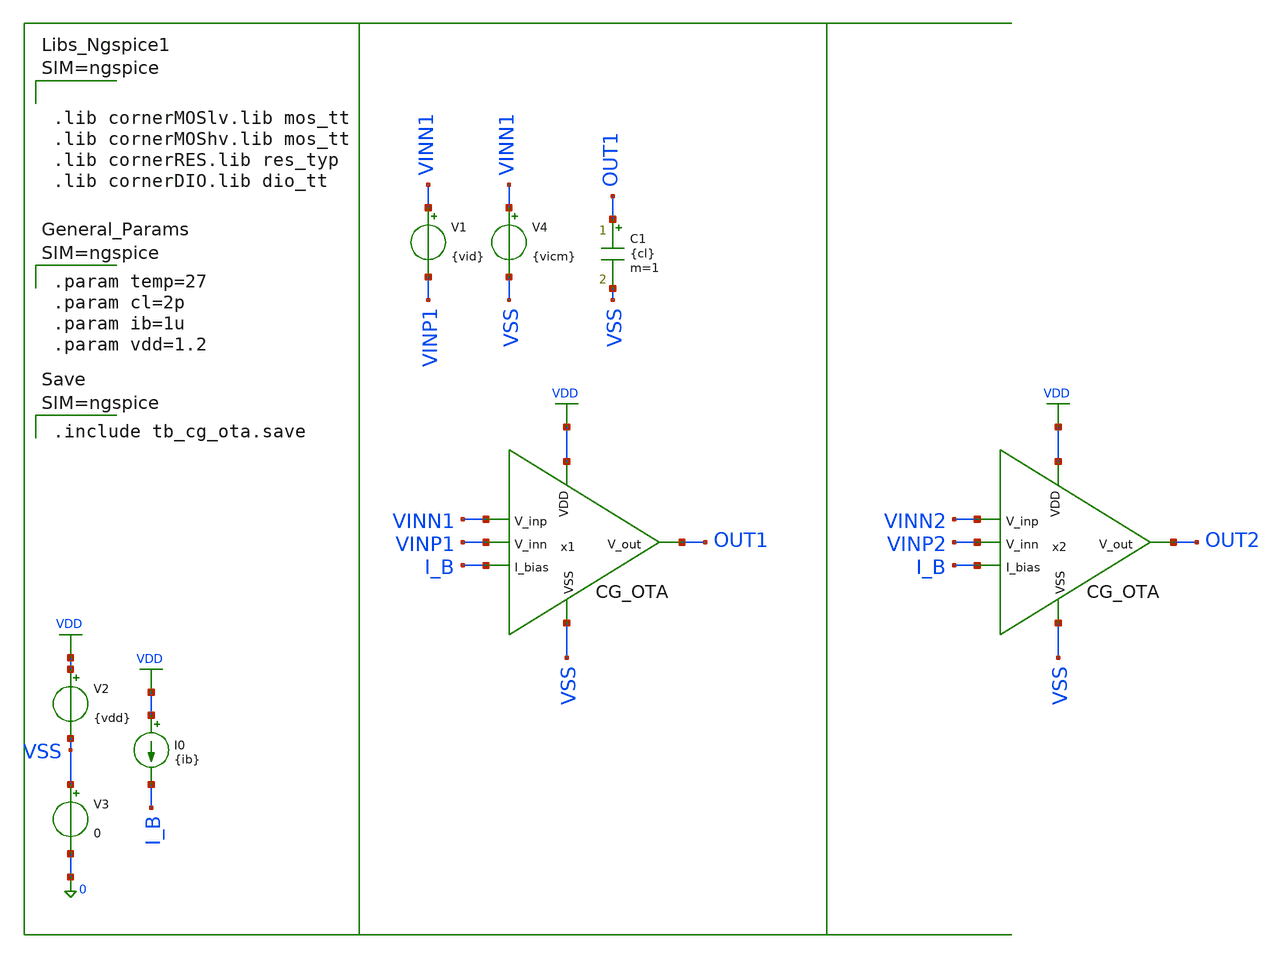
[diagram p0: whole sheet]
** sch_path: designs/libs/tb_analog/tb_cg_ota/tb_cg_ota.sch
**.subckt tb_cg_ota
x1 VDD VINN1 VINP1 OUT1 I_B VSS cg_ota
V1 VINN1 VINP1 {vid}
I0 VDD I_B {ib}
V2 VDD VSS {vdd}
V3 VSS 0 0
V4 VINN1 VSS {vicm}
C1 OUT1 VSS {cl} m=1
x2 VDD VINN2 VINP2 OUT2 I_B VSS cg_ota
**** begin user architecture code


.param temp=27
.param cl=2p
.param ib=1u
.param vdd=1.2






.param vid=0
.param vicm=0.6
.op
.control
save all
op
shell mkdir -p result
run
write ./result/tb_cg_ota_op.raw
show all : region
let i_q = -i(v2)
let p_q = i_q * 1.2
let p_q_uw = p_q * 1e6
let i_q_ua = i_q * 1e6
echo "======================================================="
echo " Quiescent Current (I_q): " $&i_q_ua " uA"
echo " Quiescent Power (P_q): " $&p_q_uw " uW"
echo "======================================================="
.endc






.lib cornerMOSlv.lib mos_tt
.lib cornerMOShv.lib mos_tt
.lib cornerRES.lib res_typ
.lib cornerDIO.lib dio_tt





.include tb_cg_ota.save




**** end user architecture code
**.ends

* expanding   symbol:
*+  /foss/designs/Programmable-Instrumentation-Amplifier-IP/designs/libs/core_analog/coarse_gain/cg_ota.sym # of pins=6
** sym_path: designs/libs/core_analog/coarse_gain/cg_ota.sym
** sch_path: designs/libs/core_analog/coarse_gain/cg_ota.sch
.subckt cg_ota VDD V_inp V_inn V_out I_bias VSS
*.ipin V_inp
*.ipin VDD
*.ipin VSS
*.opin V_out
*.ipin I_bias
*.ipin V_inn
XM1 net3 V_inp F1 VDD sg13_lv_pmos w=26.56u l=2u ng=4 m=1
XM2 net3 V_inn F2 VDD sg13_lv_pmos w=26.56u l=2u ng=4 m=1
XM3 VDD net1 net1 VDD sg13_lv_pmos w=7.33u l=2u ng=1 m=1
XM4 VDD net1 N_A VDD sg13_lv_pmos w=7.33u l=2u ng=1 m=1
XM7 F1 V_bn2 VSS VSS sg13_lv_nmos w=9.21u l=2u ng=1 m=1 mm_ok=1
XM8 F2 V_bn2 VSS VSS sg13_lv_nmos w=9.21u l=2u ng=1 m=1 mm_ok=1
XM_tail VDD net6 net3 VDD sg13_lv_pmos w=5.33u l=2u ng=1 m=4
XM_ctrlp N_A VSS N_B VDD sg13_lv_pmos w=2.20u l=0.50u ng=1 m=1
XM_outp VDD N_A V_out VDD sg13_lv_pmos w=22.20u l=0.5u ng=4 m=1
XM_ctrln N_A VDD N_B VSS sg13_lv_nmos w=0.84u l=0.5u ng=1 m=1 mm_ok=1
XM_outn V_out N_B VSS VSS sg13_lv_nmos w=8.40u l=0.5u ng=1 m=1 mm_ok=1
XC1 F2 V_out cap_cmomf w=22.58e-6 l=22.58e-6 mmin=1 mmax=4 subblock=0 rfmodel=0 subscale=1 m=1
+ mm_ok=1
XC2 N_A V_out cap_cmomf w=15.85e-6 l=15.85e-6 mmin=1 mmax=4 subblock=0 rfmodel=0 subscale=1 m=1
+ mm_ok=1
XM5 net1 V_bn1 F1 VDD sg13_lv_nmos w=6.41u l=2u ng=1 m=1 mm_ok=1
XM6 N_A V_bn1 F2 VDD sg13_lv_nmos w=6.41u l=2u ng=1 m=1 mm_ok=1
XM_mp1 VDD net2 net2 VDD sg13_lv_pmos w=2.30u l=2u ng=1 m=1
XM_mn1 net2 I_bias VSS VSS sg13_lv_nmos w=0.87u l=2u ng=1 m=1 mm_ok=1
XM_refn I_bias I_bias VSS VSS sg13_lv_nmos w=0.87u l=2u ng=1 m=1 mm_ok=1
XM_mp2 VDD net2 V_bn1 VDD sg13_lv_pmos w=11.50u l=2u ng=2 m=1
XM_mp3 VDD net2 V_bn2 VDD sg13_lv_pmos w=22.30u l=2u ng=4 m=1
XM_bn1 V_bn1 V_bn1 net4 VSS sg13_lv_nmos w=6.41u l=2u ng=1 m=1 mm_ok=1
XM_bn2 V_bn2 V_bn2 VSS VSS sg13_lv_nmos w=9.21u l=2u ng=1 m=1 mm_ok=1
XM_bn3 net4 V_bn2 VSS VSS sg13_lv_nmos w=4.61u l=2u ng=1 m=1 mm_ok=1
XM_mn2 net5 I_bias VSS VSS sg13_lv_nmos w=8.7u l=2u ng=1 m=1 mm_ok=1
XM_bp1 VDD net5 net5 VDD sg13_lv_pmos w=5.33u l=2u ng=1 m=4
XM_mn3 N_B I_bias VSS VSS sg13_lv_nmos w=2.82u l=2u ng=1 m=1 mm_ok=1
.ends

.GLOBAL VDD
.end
